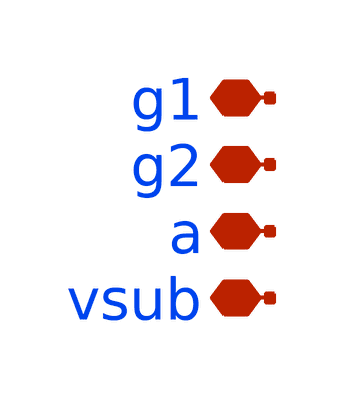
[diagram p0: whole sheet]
** sch_path: xschem/test_123.sch
**.subckt test_123 g1 g2 a vsub
*.iopin g1
*.iopin g2
*.iopin a
*.iopin vsub
**** begin user architecture code

.subckt test_123 G1 G2 A VSUBS

    X0 VSUBS G2 A VSUBS sky130_fd_pr__nfet_01v8 ad=0p pd=0u as=0p ps=0u w=1e+07u l=150000u
    X1 A G1 VSUBS VSUBS sky130_fd_pr__nfet_01v8 ad=0p pd=0u as=0p ps=0u w=1e+07u l=150000u
    C0 G1 G2 0.01fF
    C1 A G2 0.01fF
    C2 G1 A 0.02fF
    C3 A VSUBS 3.23fF $ **FLOATING
    C4 G1 VSUBS 0.26fF $ **FLOATING
    C5 G2 VSUBS 0.27fF $ **FLOATING
.ends

XDUT g1 g2 a vsubs test_123


**** end user architecture code
**.ends
.end
